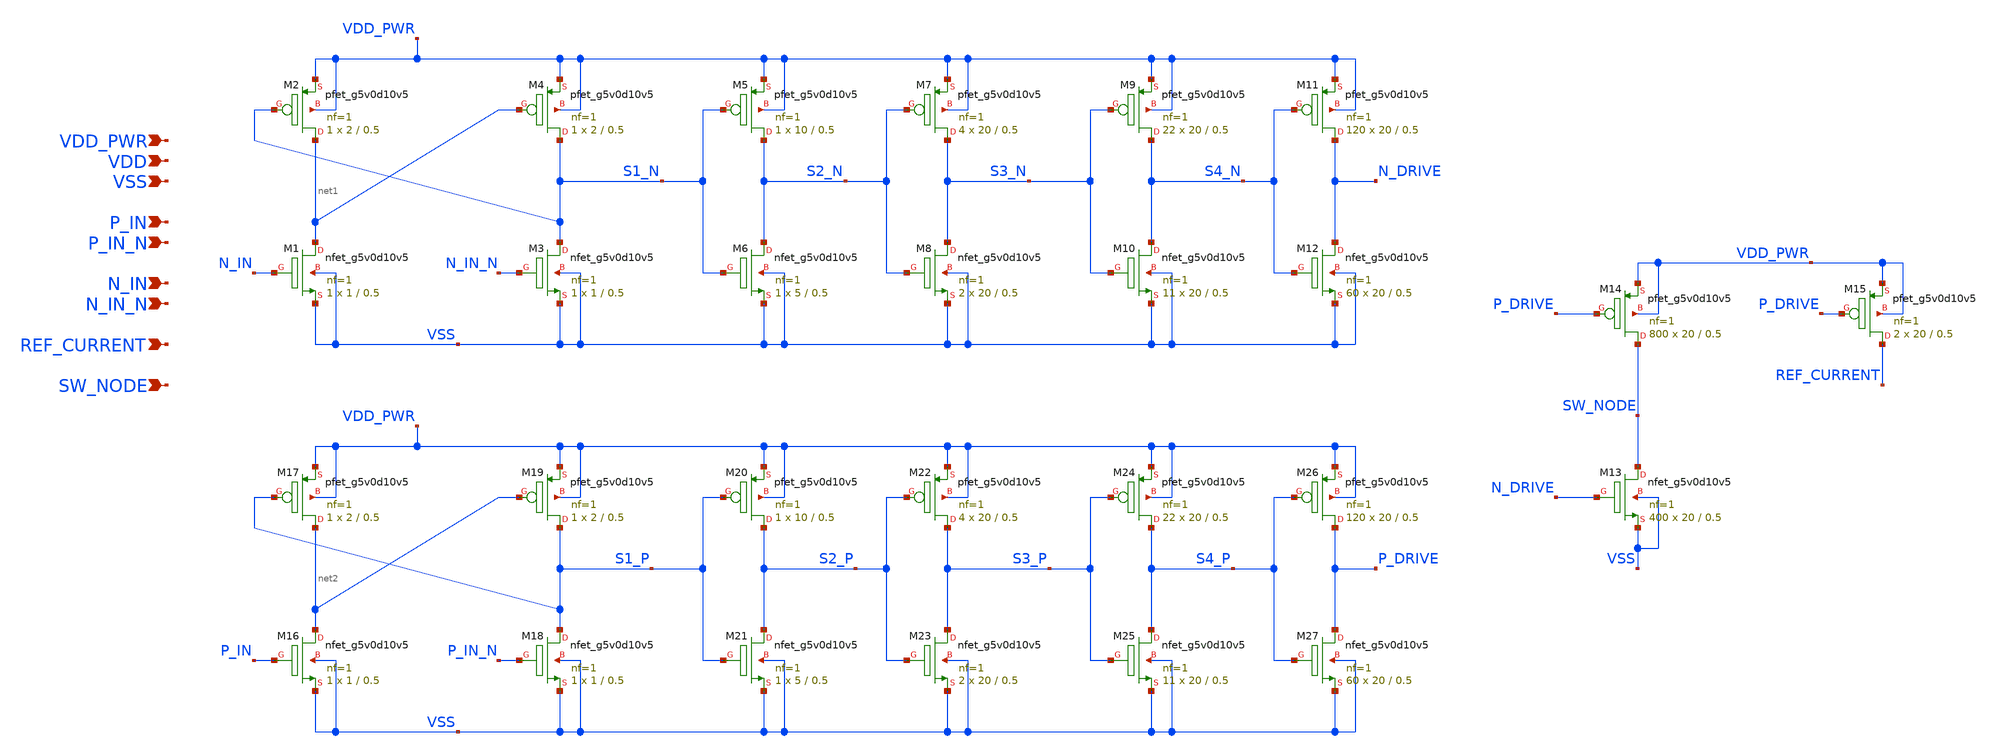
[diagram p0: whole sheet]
** sch_path: design/power-stage/power_stage.sch
**.subckt power_stage N_IN VSS VDD P_IN P_IN_N N_IN_N VDD_PWR REF_CURRENT SW_NODE
*.ipin N_IN
*.ipin VSS
*.ipin VDD
*.ipin P_IN
*.ipin P_IN_N
*.ipin N_IN_N
*.ipin VDD_PWR
*.ipin REF_CURRENT
*.ipin SW_NODE
XM1 net1 N_IN VSS VSS sky130_fd_pr__nfet_g5v0d10v5 L=0.5 W=1 nf=1 ad='int((nf+1)/2) * W/nf * 0.29' as='int((nf+2)/2) * W/nf * 0.29'
+ pd='2*int((nf+1)/2) * (W/nf + 0.29)' ps='2*int((nf+2)/2) * (W/nf + 0.29)' nrd='0.29 / W' nrs='0.29 / W'
+ sa=0 sb=0 sd=0 mult=1 m=1
XM2 net1 S1_N VDD_PWR VDD_PWR sky130_fd_pr__pfet_g5v0d10v5 L=0.5 W=2 nf=1 ad='int((nf+1)/2) * W/nf * 0.29'
+ as='int((nf+2)/2) * W/nf * 0.29' pd='2*int((nf+1)/2) * (W/nf + 0.29)' ps='2*int((nf+2)/2) * (W/nf + 0.29)'
+ nrd='0.29 / W' nrs='0.29 / W' sa=0 sb=0 sd=0 mult=1 m=1
XM3 S1_N N_IN_N VSS VSS sky130_fd_pr__nfet_g5v0d10v5 L=0.5 W=1 nf=1 ad='int((nf+1)/2) * W/nf * 0.29'
+ as='int((nf+2)/2) * W/nf * 0.29' pd='2*int((nf+1)/2) * (W/nf + 0.29)' ps='2*int((nf+2)/2) * (W/nf + 0.29)'
+ nrd='0.29 / W' nrs='0.29 / W' sa=0 sb=0 sd=0 mult=1 m=1
XM4 S1_N net1 VDD_PWR VDD_PWR sky130_fd_pr__pfet_g5v0d10v5 L=0.5 W=2 nf=1 ad='int((nf+1)/2) * W/nf * 0.29'
+ as='int((nf+2)/2) * W/nf * 0.29' pd='2*int((nf+1)/2) * (W/nf + 0.29)' ps='2*int((nf+2)/2) * (W/nf + 0.29)'
+ nrd='0.29 / W' nrs='0.29 / W' sa=0 sb=0 sd=0 mult=1 m=1
XM5 S2_N S1_N VDD_PWR VDD_PWR sky130_fd_pr__pfet_g5v0d10v5 L=0.5 W=10 nf=1 ad='int((nf+1)/2) * W/nf * 0.29'
+ as='int((nf+2)/2) * W/nf * 0.29' pd='2*int((nf+1)/2) * (W/nf + 0.29)' ps='2*int((nf+2)/2) * (W/nf + 0.29)'
+ nrd='0.29 / W' nrs='0.29 / W' sa=0 sb=0 sd=0 mult=1 m=1
XM6 S2_N S1_N VSS VSS sky130_fd_pr__nfet_g5v0d10v5 L=0.5 W=5 nf=1 ad='int((nf+1)/2) * W/nf * 0.29' as='int((nf+2)/2) * W/nf * 0.29'
+ pd='2*int((nf+1)/2) * (W/nf + 0.29)' ps='2*int((nf+2)/2) * (W/nf + 0.29)' nrd='0.29 / W' nrs='0.29 / W'
+ sa=0 sb=0 sd=0 mult=1 m=1
XM7 S3_N S2_N VDD_PWR VDD_PWR sky130_fd_pr__pfet_g5v0d10v5 L=0.5 W=20 nf=1 ad='int((nf+1)/2) * W/nf * 0.29'
+ as='int((nf+2)/2) * W/nf * 0.29' pd='2*int((nf+1)/2) * (W/nf + 0.29)' ps='2*int((nf+2)/2) * (W/nf + 0.29)'
+ nrd='0.29 / W' nrs='0.29 / W' sa=0 sb=0 sd=0 mult=4 m=4
XM8 S3_N S2_N VSS VSS sky130_fd_pr__nfet_g5v0d10v5 L=0.5 W=20 nf=1 ad='int((nf+1)/2) * W/nf * 0.29' as='int((nf+2)/2) * W/nf * 0.29'
+ pd='2*int((nf+1)/2) * (W/nf + 0.29)' ps='2*int((nf+2)/2) * (W/nf + 0.29)' nrd='0.29 / W' nrs='0.29 / W'
+ sa=0 sb=0 sd=0 mult=2 m=2
XM9 S4_N S3_N VDD_PWR VDD_PWR sky130_fd_pr__pfet_g5v0d10v5 L=0.5 W=20 nf=1 ad='int((nf+1)/2) * W/nf * 0.29'
+ as='int((nf+2)/2) * W/nf * 0.29' pd='2*int((nf+1)/2) * (W/nf + 0.29)' ps='2*int((nf+2)/2) * (W/nf + 0.29)'
+ nrd='0.29 / W' nrs='0.29 / W' sa=0 sb=0 sd=0 mult=22 m=22
XM10 S4_N S3_N VSS VSS sky130_fd_pr__nfet_g5v0d10v5 L=0.5 W=20 nf=1 ad='int((nf+1)/2) * W/nf * 0.29'
+ as='int((nf+2)/2) * W/nf * 0.29' pd='2*int((nf+1)/2) * (W/nf + 0.29)' ps='2*int((nf+2)/2) * (W/nf + 0.29)'
+ nrd='0.29 / W' nrs='0.29 / W' sa=0 sb=0 sd=0 mult=11 m=11
XM11 N_DRIVE S4_N VDD_PWR VDD_PWR sky130_fd_pr__pfet_g5v0d10v5 L=0.5 W=20 nf=1 ad='int((nf+1)/2) * W/nf * 0.29'
+ as='int((nf+2)/2) * W/nf * 0.29' pd='2*int((nf+1)/2) * (W/nf + 0.29)' ps='2*int((nf+2)/2) * (W/nf + 0.29)'
+ nrd='0.29 / W' nrs='0.29 / W' sa=0 sb=0 sd=0 mult=120 m=120
XM12 N_DRIVE S4_N VSS VSS sky130_fd_pr__nfet_g5v0d10v5 L=0.5 W=20 nf=1 ad='int((nf+1)/2) * W/nf * 0.29'
+ as='int((nf+2)/2) * W/nf * 0.29' pd='2*int((nf+1)/2) * (W/nf + 0.29)' ps='2*int((nf+2)/2) * (W/nf + 0.29)'
+ nrd='0.29 / W' nrs='0.29 / W' sa=0 sb=0 sd=0 mult=60 m=60
XM13 SW_NODE N_DRIVE VSS VSS sky130_fd_pr__nfet_g5v0d10v5 L=0.5 W=20 nf=1 ad='int((nf+1)/2) * W/nf * 0.29'
+ as='int((nf+2)/2) * W/nf * 0.29' pd='2*int((nf+1)/2) * (W/nf + 0.29)' ps='2*int((nf+2)/2) * (W/nf + 0.29)'
+ nrd='0.29 / W' nrs='0.29 / W' sa=0 sb=0 sd=0 mult=400 m=400
XM14 SW_NODE P_DRIVE VDD_PWR VDD_PWR sky130_fd_pr__pfet_g5v0d10v5 L=0.5 W=20 nf=1 ad='int((nf+1)/2) * W/nf * 0.29'
+ as='int((nf+2)/2) * W/nf * 0.29' pd='2*int((nf+1)/2) * (W/nf + 0.29)' ps='2*int((nf+2)/2) * (W/nf + 0.29)'
+ nrd='0.29 / W' nrs='0.29 / W' sa=0 sb=0 sd=0 mult=800 m=800
XM15 REF_CURRENT P_DRIVE VDD_PWR VDD_PWR sky130_fd_pr__pfet_g5v0d10v5 L=0.5 W=20 nf=1 ad='int((nf+1)/2) * W/nf * 0.29'
+ as='int((nf+2)/2) * W/nf * 0.29' pd='2*int((nf+1)/2) * (W/nf + 0.29)' ps='2*int((nf+2)/2) * (W/nf + 0.29)'
+ nrd='0.29 / W' nrs='0.29 / W' sa=0 sb=0 sd=0 mult=2 m=2
XM16 net2 P_IN VSS VSS sky130_fd_pr__nfet_g5v0d10v5 L=0.5 W=1 nf=1 ad='int((nf+1)/2) * W/nf * 0.29' as='int((nf+2)/2) * W/nf * 0.29'
+ pd='2*int((nf+1)/2) * (W/nf + 0.29)' ps='2*int((nf+2)/2) * (W/nf + 0.29)' nrd='0.29 / W' nrs='0.29 / W'
+ sa=0 sb=0 sd=0 mult=1 m=1
XM17 net2 S1_P VDD_PWR VDD_PWR sky130_fd_pr__pfet_g5v0d10v5 L=0.5 W=2 nf=1 ad='int((nf+1)/2) * W/nf * 0.29'
+ as='int((nf+2)/2) * W/nf * 0.29' pd='2*int((nf+1)/2) * (W/nf + 0.29)' ps='2*int((nf+2)/2) * (W/nf + 0.29)'
+ nrd='0.29 / W' nrs='0.29 / W' sa=0 sb=0 sd=0 mult=1 m=1
XM18 S1_P P_IN_N VSS VSS sky130_fd_pr__nfet_g5v0d10v5 L=0.5 W=1 nf=1 ad='int((nf+1)/2) * W/nf * 0.29'
+ as='int((nf+2)/2) * W/nf * 0.29' pd='2*int((nf+1)/2) * (W/nf + 0.29)' ps='2*int((nf+2)/2) * (W/nf + 0.29)'
+ nrd='0.29 / W' nrs='0.29 / W' sa=0 sb=0 sd=0 mult=1 m=1
XM19 S1_P net2 VDD_PWR VDD_PWR sky130_fd_pr__pfet_g5v0d10v5 L=0.5 W=2 nf=1 ad='int((nf+1)/2) * W/nf * 0.29'
+ as='int((nf+2)/2) * W/nf * 0.29' pd='2*int((nf+1)/2) * (W/nf + 0.29)' ps='2*int((nf+2)/2) * (W/nf + 0.29)'
+ nrd='0.29 / W' nrs='0.29 / W' sa=0 sb=0 sd=0 mult=1 m=1
XM20 S2_P S1_P VDD_PWR VDD_PWR sky130_fd_pr__pfet_g5v0d10v5 L=0.5 W=10 nf=1 ad='int((nf+1)/2) * W/nf * 0.29'
+ as='int((nf+2)/2) * W/nf * 0.29' pd='2*int((nf+1)/2) * (W/nf + 0.29)' ps='2*int((nf+2)/2) * (W/nf + 0.29)'
+ nrd='0.29 / W' nrs='0.29 / W' sa=0 sb=0 sd=0 mult=1 m=1
XM21 S2_P S1_P VSS VSS sky130_fd_pr__nfet_g5v0d10v5 L=0.5 W=5 nf=1 ad='int((nf+1)/2) * W/nf * 0.29' as='int((nf+2)/2) * W/nf * 0.29'
+ pd='2*int((nf+1)/2) * (W/nf + 0.29)' ps='2*int((nf+2)/2) * (W/nf + 0.29)' nrd='0.29 / W' nrs='0.29 / W'
+ sa=0 sb=0 sd=0 mult=1 m=1
XM22 S3_P S2_P VDD_PWR VDD_PWR sky130_fd_pr__pfet_g5v0d10v5 L=0.5 W=20 nf=1 ad='int((nf+1)/2) * W/nf * 0.29'
+ as='int((nf+2)/2) * W/nf * 0.29' pd='2*int((nf+1)/2) * (W/nf + 0.29)' ps='2*int((nf+2)/2) * (W/nf + 0.29)'
+ nrd='0.29 / W' nrs='0.29 / W' sa=0 sb=0 sd=0 mult=4 m=4
XM23 S3_P S2_P VSS VSS sky130_fd_pr__nfet_g5v0d10v5 L=0.5 W=20 nf=1 ad='int((nf+1)/2) * W/nf * 0.29'
+ as='int((nf+2)/2) * W/nf * 0.29' pd='2*int((nf+1)/2) * (W/nf + 0.29)' ps='2*int((nf+2)/2) * (W/nf + 0.29)'
+ nrd='0.29 / W' nrs='0.29 / W' sa=0 sb=0 sd=0 mult=2 m=2
XM24 S4_P S3_P VDD_PWR VDD_PWR sky130_fd_pr__pfet_g5v0d10v5 L=0.5 W=20 nf=1 ad='int((nf+1)/2) * W/nf * 0.29'
+ as='int((nf+2)/2) * W/nf * 0.29' pd='2*int((nf+1)/2) * (W/nf + 0.29)' ps='2*int((nf+2)/2) * (W/nf + 0.29)'
+ nrd='0.29 / W' nrs='0.29 / W' sa=0 sb=0 sd=0 mult=22 m=22
XM25 S4_P S3_P VSS VSS sky130_fd_pr__nfet_g5v0d10v5 L=0.5 W=20 nf=1 ad='int((nf+1)/2) * W/nf * 0.29'
+ as='int((nf+2)/2) * W/nf * 0.29' pd='2*int((nf+1)/2) * (W/nf + 0.29)' ps='2*int((nf+2)/2) * (W/nf + 0.29)'
+ nrd='0.29 / W' nrs='0.29 / W' sa=0 sb=0 sd=0 mult=11 m=11
XM26 P_DRIVE S4_P VDD_PWR VDD_PWR sky130_fd_pr__pfet_g5v0d10v5 L=0.5 W=20 nf=1 ad='int((nf+1)/2) * W/nf * 0.29'
+ as='int((nf+2)/2) * W/nf * 0.29' pd='2*int((nf+1)/2) * (W/nf + 0.29)' ps='2*int((nf+2)/2) * (W/nf + 0.29)'
+ nrd='0.29 / W' nrs='0.29 / W' sa=0 sb=0 sd=0 mult=120 m=120
XM27 P_DRIVE S4_P VSS VSS sky130_fd_pr__nfet_g5v0d10v5 L=0.5 W=20 nf=1 ad='int((nf+1)/2) * W/nf * 0.29'
+ as='int((nf+2)/2) * W/nf * 0.29' pd='2*int((nf+1)/2) * (W/nf + 0.29)' ps='2*int((nf+2)/2) * (W/nf + 0.29)'
+ nrd='0.29 / W' nrs='0.29 / W' sa=0 sb=0 sd=0 mult=60 m=60
**.ends
.end
